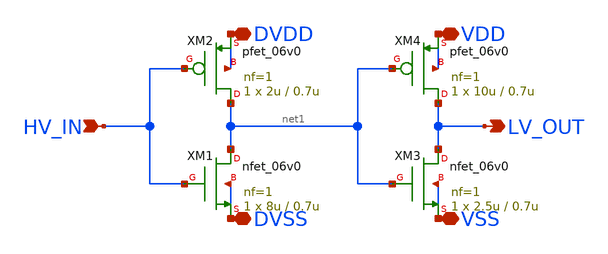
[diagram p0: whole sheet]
** sch_path: shifters/basic_shifter_hl.sch
**.subckt basic_shifter_hl HV_IN LV_OUT DVDD DVSS VDD VSS
*.ipin HV_IN
*.opin LV_OUT
*.iopin DVDD
*.iopin DVSS
*.iopin VDD
*.iopin VSS
XM1 net1 HV_IN DVSS DVSS nfet_06v0 L=0.7u W=8u nf=1 ad='int((nf+1)/2) * W/nf * 0.18u' as='int((nf+2)/2) * W/nf * 0.18u'
+ pd='2*int((nf+1)/2) * (W/nf + 0.18u)' ps='2*int((nf+2)/2) * (W/nf + 0.18u)' nrd='0.18u / W' nrs='0.18u / W'
+ sa=0 sb=0 sd=0 m=1
XM2 net1 HV_IN DVDD DVDD pfet_06v0 L=0.7u W=2u nf=1 ad='int((nf+1)/2) * W/nf * 0.18u' as='int((nf+2)/2) * W/nf * 0.18u'
+ pd='2*int((nf+1)/2) * (W/nf + 0.18u)' ps='2*int((nf+2)/2) * (W/nf + 0.18u)' nrd='0.18u / W' nrs='0.18u / W'
+ sa=0 sb=0 sd=0 m=1
XM3 LV_OUT net1 VSS VSS nfet_06v0 L=0.7u W=2.5u nf=1 ad='int((nf+1)/2) * W/nf * 0.18u' as='int((nf+2)/2) * W/nf * 0.18u'
+ pd='2*int((nf+1)/2) * (W/nf + 0.18u)' ps='2*int((nf+2)/2) * (W/nf + 0.18u)' nrd='0.18u / W' nrs='0.18u / W'
+ sa=0 sb=0 sd=0 m=1
XM4 LV_OUT net1 VDD VDD pfet_06v0 L=0.7u W=10u nf=1 ad='int((nf+1)/2) * W/nf * 0.18u' as='int((nf+2)/2) * W/nf * 0.18u'
+ pd='2*int((nf+1)/2) * (W/nf + 0.18u)' ps='2*int((nf+2)/2) * (W/nf + 0.18u)' nrd='0.18u / W' nrs='0.18u / W'
+ sa=0 sb=0 sd=0 m=1
**.ends
.end
